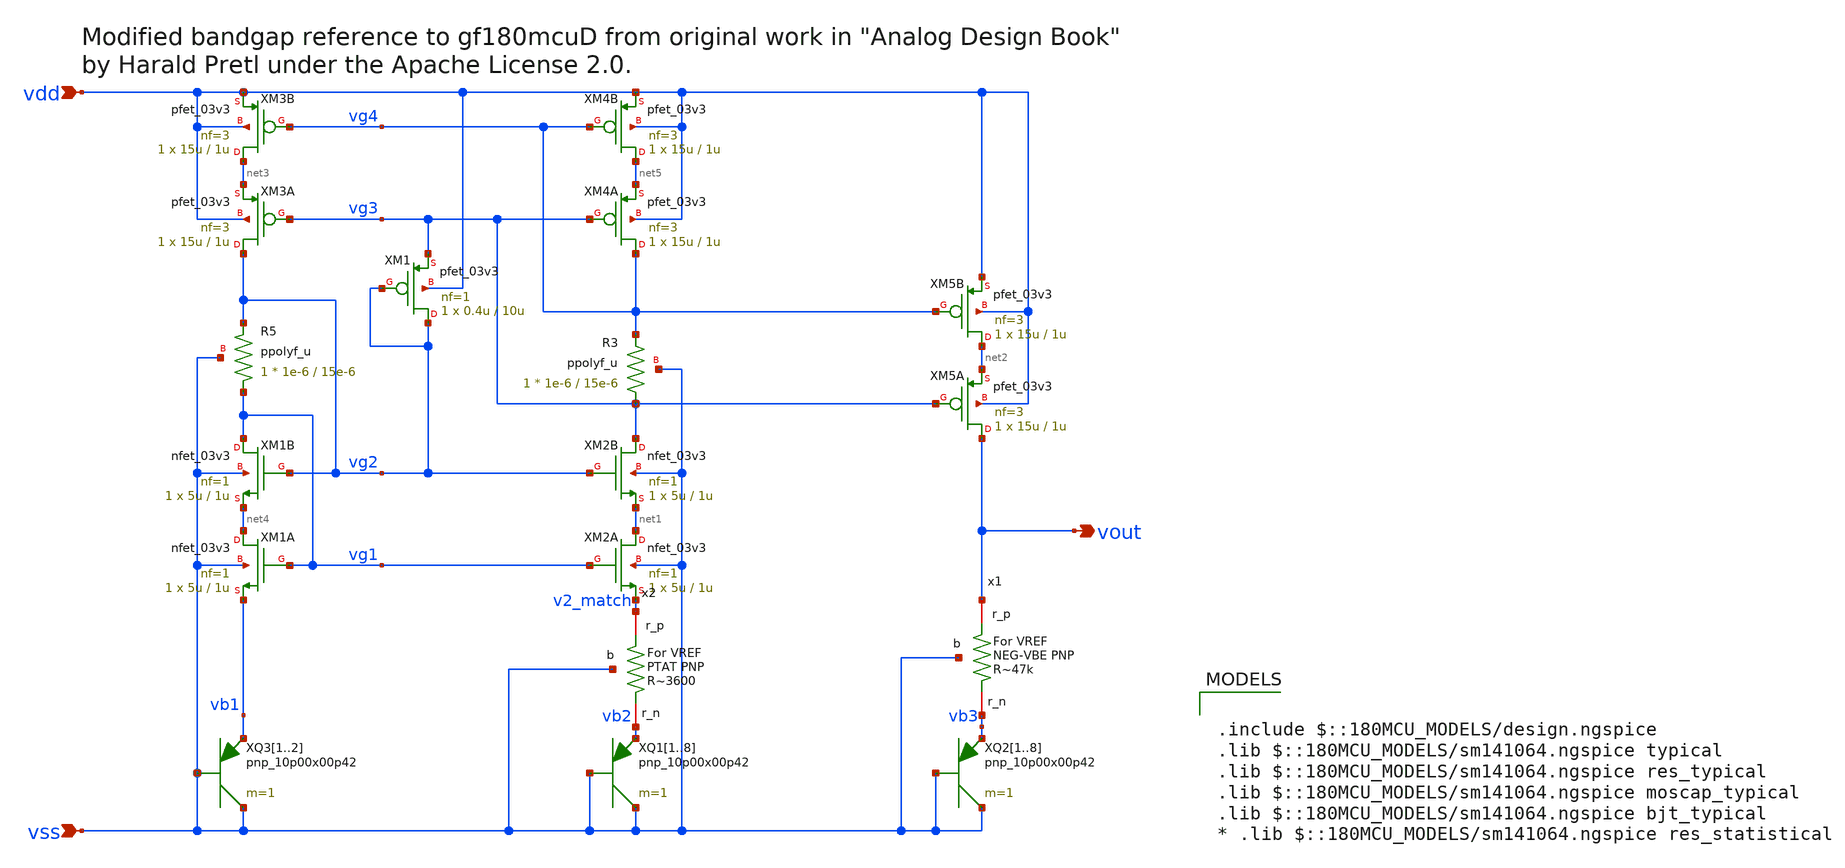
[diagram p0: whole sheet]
** sch_path: designs/libs/core_analog/vref/voltage_reference.sch
* by Harald Pretl under the Apache License 2.0.
**.subckt voltage_reference vdd vout vss
*.ipin vdd
*.opin vout
*.ipin vss
XM1B vg1 vg2 net4 vss nfet_03v3 L=1u W=5u nf=1 ad='int((nf+1)/2) * W/nf * 0.18u' as='int((nf+2)/2) * W/nf * 0.18u'
+ pd='2*int((nf+1)/2) * (W/nf + 0.18u)' ps='2*int((nf+2)/2) * (W/nf + 0.18u)' nrd='0.18u / W' nrs='0.18u / W'
+ sa=0 sb=0 sd=0 m=1
XM1A net4 vg1 vb1 vss nfet_03v3 L=1u W=5u nf=1 ad='int((nf+1)/2) * W/nf * 0.18u' as='int((nf+2)/2) * W/nf * 0.18u'
+ pd='2*int((nf+1)/2) * (W/nf + 0.18u)' ps='2*int((nf+2)/2) * (W/nf + 0.18u)' nrd='0.18u / W' nrs='0.18u / W'
+ sa=0 sb=0 sd=0 m=1
XM2B vg3 vg2 net1 vss nfet_03v3 L=1u W=5u nf=1 ad='int((nf+1)/2) * W/nf * 0.18u' as='int((nf+2)/2) * W/nf * 0.18u'
+ pd='2*int((nf+1)/2) * (W/nf + 0.18u)' ps='2*int((nf+2)/2) * (W/nf + 0.18u)' nrd='0.18u / W' nrs='0.18u / W'
+ sa=0 sb=0 sd=0 m=1
XM2A net1 vg1 v2_match vss nfet_03v3 L=1u W=5u nf=1 ad='int((nf+1)/2) * W/nf * 0.18u' as='int((nf+2)/2) * W/nf * 0.18u'
+ pd='2*int((nf+1)/2) * (W/nf + 0.18u)' ps='2*int((nf+2)/2) * (W/nf + 0.18u)' nrd='0.18u / W' nrs='0.18u / W'
+ sa=0 sb=0 sd=0 m=1
XM4A vg4 vg3 net5 vdd pfet_03v3 L=1u W=15u nf=3 ad='int((nf+1)/2) * W/nf * 0.18u' as='int((nf+2)/2) * W/nf * 0.18u'
+ pd='2*int((nf+1)/2) * (W/nf + 0.18u)' ps='2*int((nf+2)/2) * (W/nf + 0.18u)' nrd='0.18u / W' nrs='0.18u / W'
+ sa=0 sb=0 sd=0 m=1
XM4B net5 vg4 vdd vdd pfet_03v3 L=1u W=15u nf=3 ad='int((nf+1)/2) * W/nf * 0.18u' as='int((nf+2)/2) * W/nf * 0.18u'
+ pd='2*int((nf+1)/2) * (W/nf + 0.18u)' ps='2*int((nf+2)/2) * (W/nf + 0.18u)' nrd='0.18u / W' nrs='0.18u / W'
+ sa=0 sb=0 sd=0 m=1
XM3A vg2 vg3 net3 vdd pfet_03v3 L=1u W=15u nf=3 ad='int((nf+1)/2) * W/nf * 0.18u' as='int((nf+2)/2) * W/nf * 0.18u'
+ pd='2*int((nf+1)/2) * (W/nf + 0.18u)' ps='2*int((nf+2)/2) * (W/nf + 0.18u)' nrd='0.18u / W' nrs='0.18u / W'
+ sa=0 sb=0 sd=0 m=1
XM3B net3 vg4 vdd vdd pfet_03v3 L=1u W=15u nf=3 ad='int((nf+1)/2) * W/nf * 0.18u' as='int((nf+2)/2) * W/nf * 0.18u'
+ pd='2*int((nf+1)/2) * (W/nf + 0.18u)' ps='2*int((nf+2)/2) * (W/nf + 0.18u)' nrd='0.18u / W' nrs='0.18u / W'
+ sa=0 sb=0 sd=0 m=1
XM5A vout vg3 net2 vdd pfet_03v3 L=1u W=15u nf=3 ad='int((nf+1)/2) * W/nf * 0.18u' as='int((nf+2)/2) * W/nf * 0.18u'
+ pd='2*int((nf+1)/2) * (W/nf + 0.18u)' ps='2*int((nf+2)/2) * (W/nf + 0.18u)' nrd='0.18u / W' nrs='0.18u / W'
+ sa=0 sb=0 sd=0 m=1
XM5B net2 vg4 vdd vdd pfet_03v3 L=1u W=15u nf=3 ad='int((nf+1)/2) * W/nf * 0.18u' as='int((nf+2)/2) * W/nf * 0.18u'
+ pd='2*int((nf+1)/2) * (W/nf + 0.18u)' ps='2*int((nf+2)/2) * (W/nf + 0.18u)' nrd='0.18u / W' nrs='0.18u / W'
+ sa=0 sb=0 sd=0 m=1
XQ11 vss vss vb2 pnp_10p00x00p42 m=1 par=1
XQ12 vss vss vb2 pnp_10p00x00p42 m=1 par=1
XQ13 vss vss vb2 pnp_10p00x00p42 m=1 par=1
XQ14 vss vss vb2 pnp_10p00x00p42 m=1 par=1
XQ15 vss vss vb2 pnp_10p00x00p42 m=1 par=1
XQ16 vss vss vb2 pnp_10p00x00p42 m=1 par=1
XQ17 vss vss vb2 pnp_10p00x00p42 m=1 par=1
XQ18 vss vss vb2 pnp_10p00x00p42 m=1 par=1
XQ21 vss vss vb3 pnp_10p00x00p42 m=1 par=1
XQ22 vss vss vb3 pnp_10p00x00p42 m=1 par=1
XQ23 vss vss vb3 pnp_10p00x00p42 m=1 par=1
XQ24 vss vss vb3 pnp_10p00x00p42 m=1 par=1
XQ25 vss vss vb3 pnp_10p00x00p42 m=1 par=1
XQ26 vss vss vb3 pnp_10p00x00p42 m=1 par=1
XQ27 vss vss vb3 pnp_10p00x00p42 m=1 par=1
XQ28 vss vss vb3 pnp_10p00x00p42 m=1 par=1
XQ31 vss vss vb1 pnp_10p00x00p42 m=1 par=1
XQ32 vss vss vb1 pnp_10p00x00p42 m=1 par=1
XM1 vg2 vg2 vg3 vdd pfet_03v3 L=10u W=0.4u nf=1 ad='int((nf+1)/2) * W/nf * 0.18u' as='int((nf+2)/2) * W/nf * 0.18u'
+ pd='2*int((nf+1)/2) * (W/nf + 0.18u)' ps='2*int((nf+2)/2) * (W/nf + 0.18u)' nrd='0.18u / W' nrs='0.18u / W'
+ sa=0 sb=0 sd=0 m=1
XR3 vg3 vg4 vss ppolyf_u r_width=1e-6 r_length=15e-6 m=1
XR5 vg1 vg2 vss ppolyf_u r_width=1e-6 r_length=15e-6 m=1
x1 vout vss vb3 vref_R2
x2 v2_match vss vb2 vref_R1
**** begin user architecture code

.include $::180MCU_MODELS/design.ngspice
.lib $::180MCU_MODELS/sm141064.ngspice typical
.lib $::180MCU_MODELS/sm141064.ngspice res_typical
.lib $::180MCU_MODELS/sm141064.ngspice moscap_typical
.lib $::180MCU_MODELS/sm141064.ngspice bjt_typical
* .lib $::180MCU_MODELS/sm141064.ngspice res_statistical

**** end user architecture code
**.ends

* expanding   symbol:  libs/core_analog/vref/vref_R2.sym # of pins=3
** sym_path: designs/libs/core_analog/vref/vref_R2.sym
** sch_path: designs/libs/core_analog/vref/vref_R2.sch
.subckt vref_R2 r_p b r_n
*.iopin r_p
*.iopin r_n
*.iopin b
XR1 net1 net3 b ppolyf_u r_width=2.5e-6 r_length=25e-6 m=1
XR2 net2 net4 b ppolyf_u r_width=2.5e-6 r_length=25e-6 m=1
XR3 r_n net1 b ppolyf_u r_width=2.5e-6 r_length=25e-6 m=1
XR4 net3 net2 b ppolyf_u r_width=2.5e-6 r_length=25e-6 m=1
XR5 net5 net6 b ppolyf_u r_width=2.5e-6 r_length=25e-6 m=1
XR7 net4 net5 b ppolyf_u r_width=2.5e-6 r_length=25e-6 m=1
XR8 net6 net12 b ppolyf_u r_width=2.5e-6 r_length=25e-6 m=1
XR6 net12 net7 b ppolyf_u r_width=2.5e-6 r_length=25e-6 m=1
XR9 net8 net10 b ppolyf_u r_width=2.5e-6 r_length=25e-6 m=1
XR10 net9 net11 b ppolyf_u r_width=2.5e-6 r_length=25e-6 m=1
XR11 net7 net8 b ppolyf_u r_width=2.5e-6 r_length=25e-6 m=1
XR12 net10 net9 b ppolyf_u r_width=2.5e-6 r_length=25e-6 m=1
XR13 net11 r_p b ppolyf_u r_width=2.5e-6 r_length=25e-6 m=1
.ends


* expanding   symbol:  libs/core_analog/vref/vref_R1.sym # of pins=3
** sym_path: designs/libs/core_analog/vref/vref_R1.sym
** sch_path: designs/libs/core_analog/vref/vref_R1.sch
.subckt vref_R1 r_p b r_n
*.iopin r_p
*.iopin r_n
*.iopin b
XR1 net1 r_p b ppolyf_u r_width=2.5e-6 r_length=25e-6 m=1
XR2 net2 r_p b ppolyf_u r_width=2.5e-6 r_length=25e-6 m=1
XR3 r_n net1 b ppolyf_u r_width=2.5e-6 r_length=25e-6 m=1
XR4 r_n net2 b ppolyf_u r_width=2.5e-6 r_length=25e-6 m=1
.ends

.end
